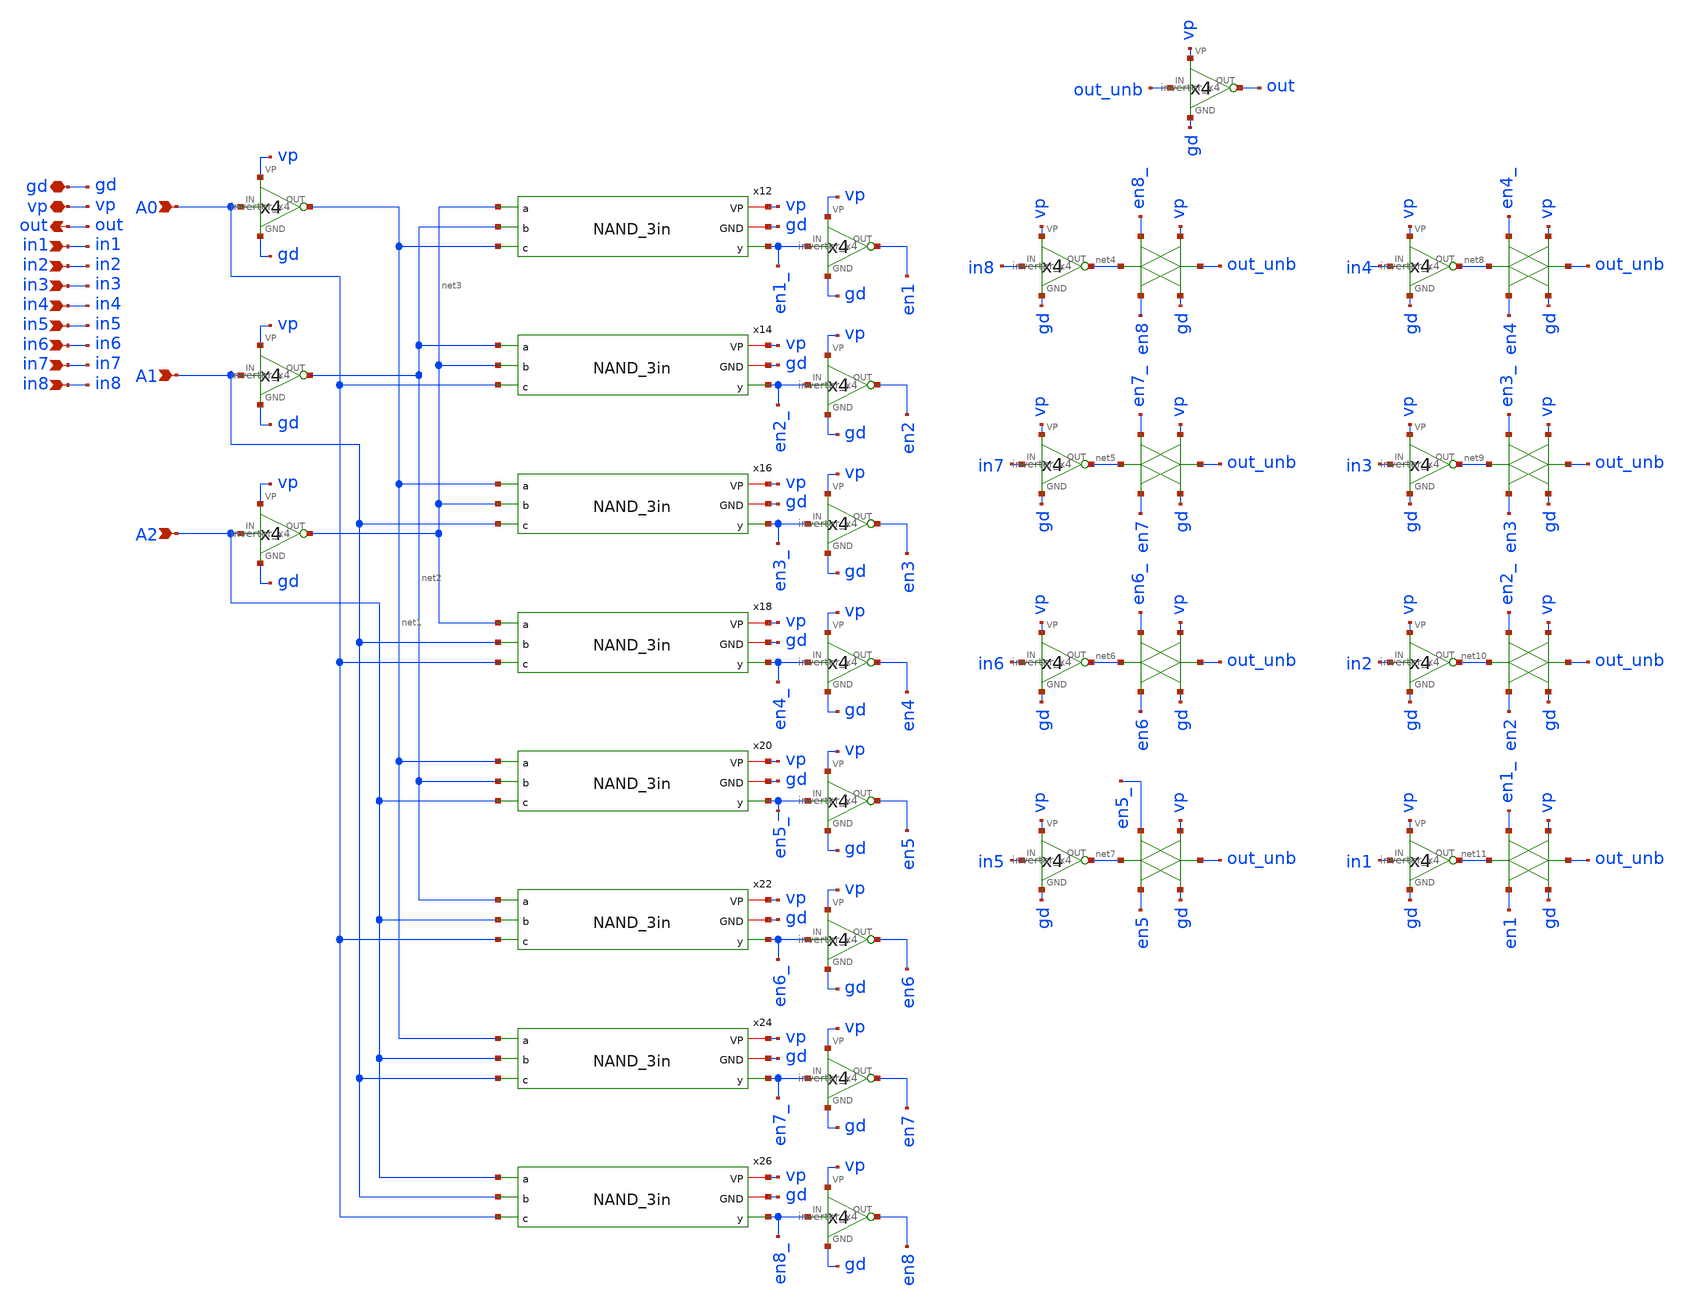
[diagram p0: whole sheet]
** sch_path: PLL0663-main/schematic/xschem/divider/MUX_8to1.sch
**.subckt MUX_8to1 gd vp out in1 in2 in3 in4 in5 in6 in7 in8 A0 A1 A2
*.iopin gd
*.iopin vp
*.opin out
*.ipin in1
*.ipin in2
*.ipin in3
*.ipin in4
*.ipin in5
*.ipin in6
*.ipin in7
*.ipin in8
*.ipin A0
*.ipin A1
*.ipin A2
x9 A0 net1 vp gd inverter_x4
x10 A1 net2 vp gd inverter_x4
x11 A2 net3 vp gd inverter_x4
x28 out_unb out vp gd inverter_x4
x29 in4 net8 vp gd inverter_x4
x30 in8 net4 vp gd inverter_x4
x31 in7 net5 vp gd inverter_x4
x32 in6 net6 vp gd inverter_x4
x33 in5 net7 vp gd inverter_x4
x34 in1 net11 vp gd inverter_x4
x35 in2 net10 vp gd inverter_x4
x36 in3 net9 vp gd inverter_x4
x13 en1_ en1 vp gd inverter_x4
x15 en2_ en2 vp gd inverter_x4
x17 en3_ en3 vp gd inverter_x4
x19 en4_ en4 vp gd inverter_x4
x21 en5_ en5 vp gd inverter_x4
x23 en6_ en6 vp gd inverter_x4
x25 en7_ en7 vp gd inverter_x4
x27 en8_ en8 vp gd inverter_x4
x12 vp gd net3 en1_ net2 net1 NAND_3in
x14 vp gd net2 en2_ net3 A0 NAND_3in
x16 vp gd net1 en3_ net3 A1 NAND_3in
x18 vp gd net3 en4_ A1 A0 NAND_3in
x20 vp gd net1 en5_ net2 A2 NAND_3in
x22 vp gd net2 en6_ A2 A0 NAND_3in
x24 vp gd net1 en7_ A2 A1 NAND_3in
x26 vp gd A2 en8_ A1 A0 NAND_3in
**.ends
.end
